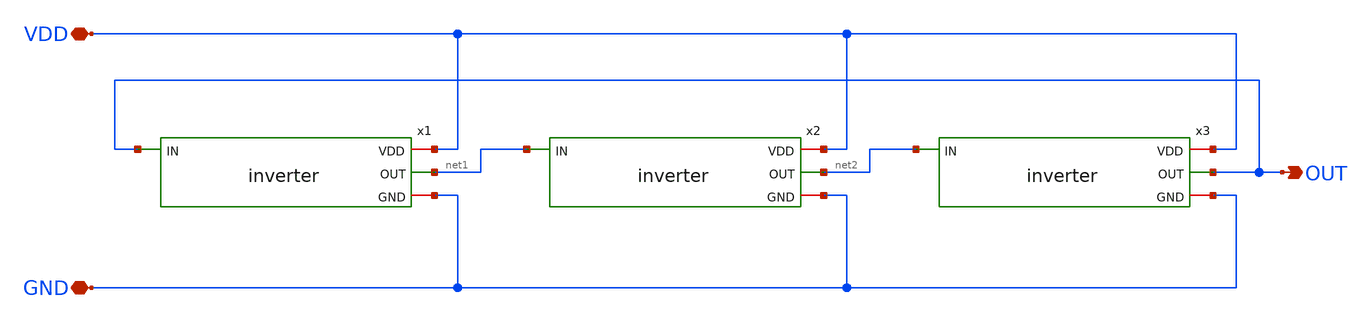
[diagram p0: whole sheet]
** sch_path: ring_oscillator/ring_oscillator.sch
**.subckt ring_oscillator VDD GND OUT
*.iopin VDD
*.iopin GND
*.opin OUT
x1 VDD OUT net1 GND inverter
x2 VDD net1 net2 GND inverter
x3 VDD net2 OUT GND inverter
**.ends

* expanding   symbol:  inverter.sym # of pins=4
** sym_path: ring_oscillator/inverter.sym
** sch_path: ring_oscillator/inverter.sch
.subckt inverter VDD IN OUT GND
*.ipin IN
*.iopin VDD
*.iopin GND
*.opin OUT
XM1 OUT IN GND GND sky130_fd_pr__nfet_01v8 L=0.15 W=1 nf=1 ad='int((nf+1)/2) * W/nf * 0.29' as='int((nf+2)/2) * W/nf * 0.29'
+ pd='2*int((nf+1)/2) * (W/nf + 0.29)' ps='2*int((nf+2)/2) * (W/nf + 0.29)' nrd='0.29 / W' nrs='0.29 / W'
+ sa=0 sb=0 sd=0 mult=1 m=1
XM2 OUT IN VDD VDD sky130_fd_pr__pfet_01v8 L=0.15 W=1 nf=1 ad='int((nf+1)/2) * W/nf * 0.29' as='int((nf+2)/2) * W/nf * 0.29'
+ pd='2*int((nf+1)/2) * (W/nf + 0.29)' ps='2*int((nf+2)/2) * (W/nf + 0.29)' nrd='0.29 / W' nrs='0.29 / W'
+ sa=0 sb=0 sd=0 mult=1 m=1
.ends

.end
